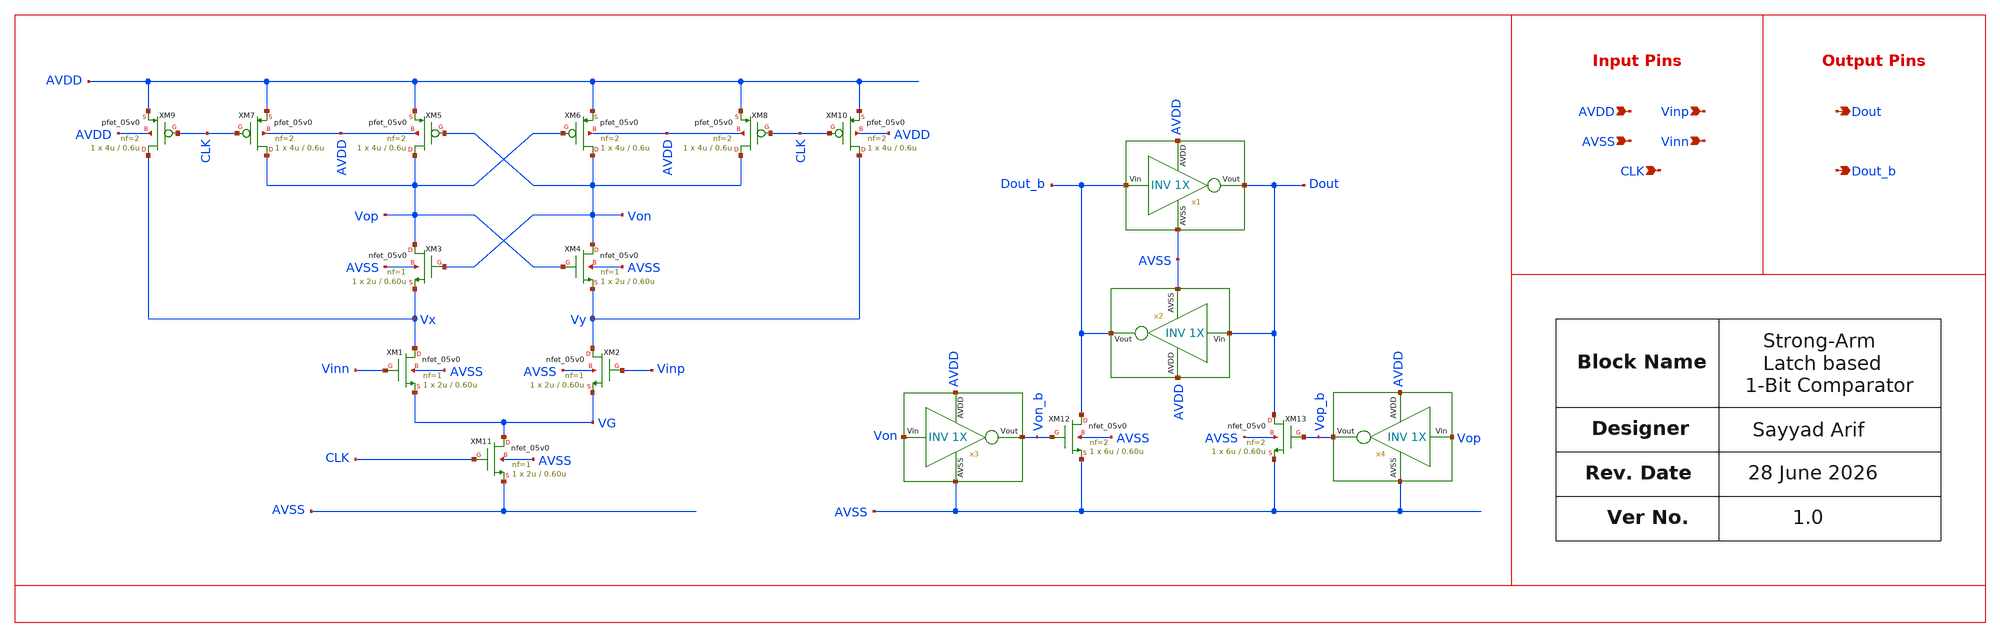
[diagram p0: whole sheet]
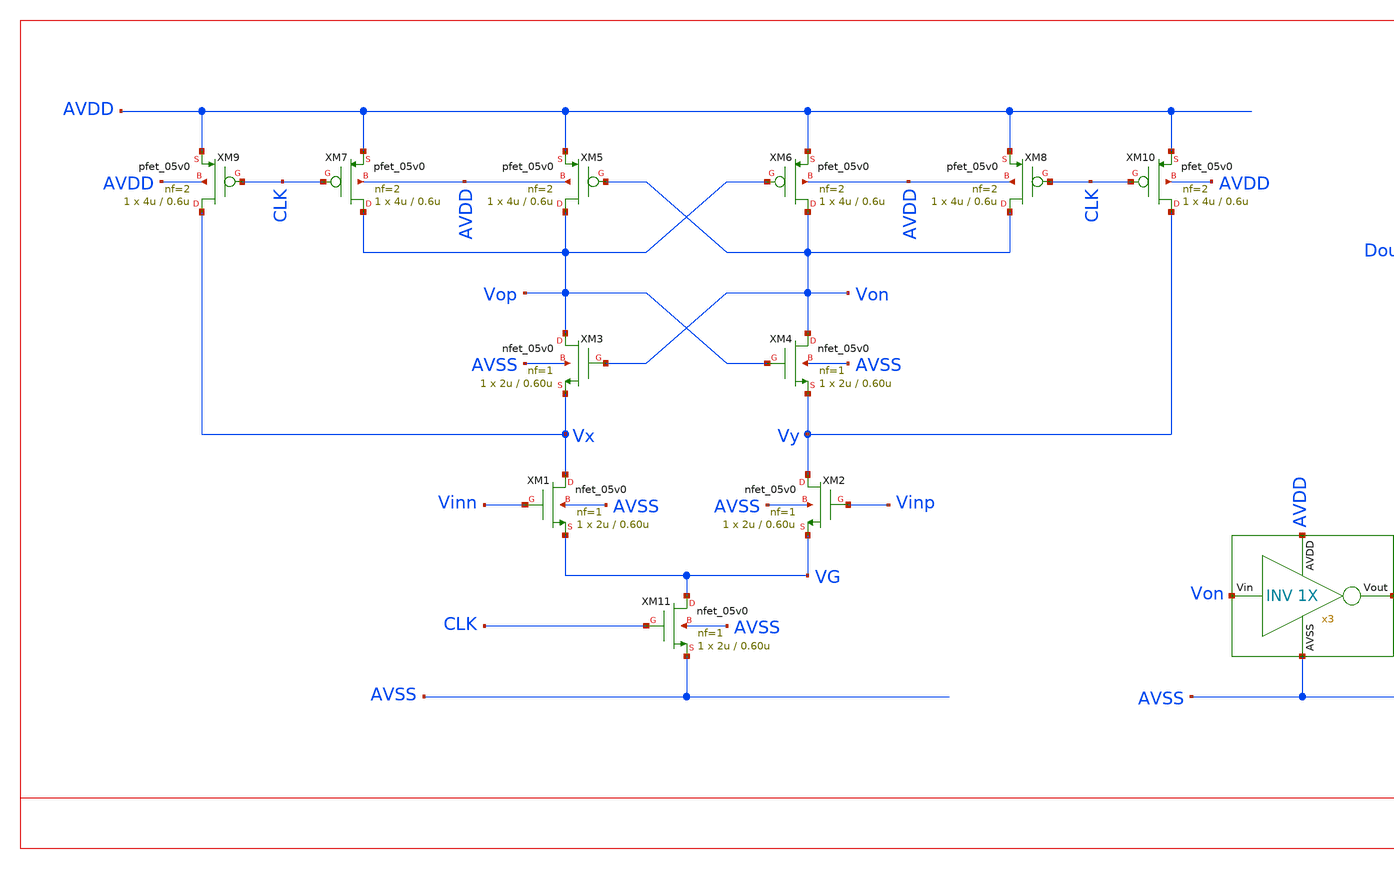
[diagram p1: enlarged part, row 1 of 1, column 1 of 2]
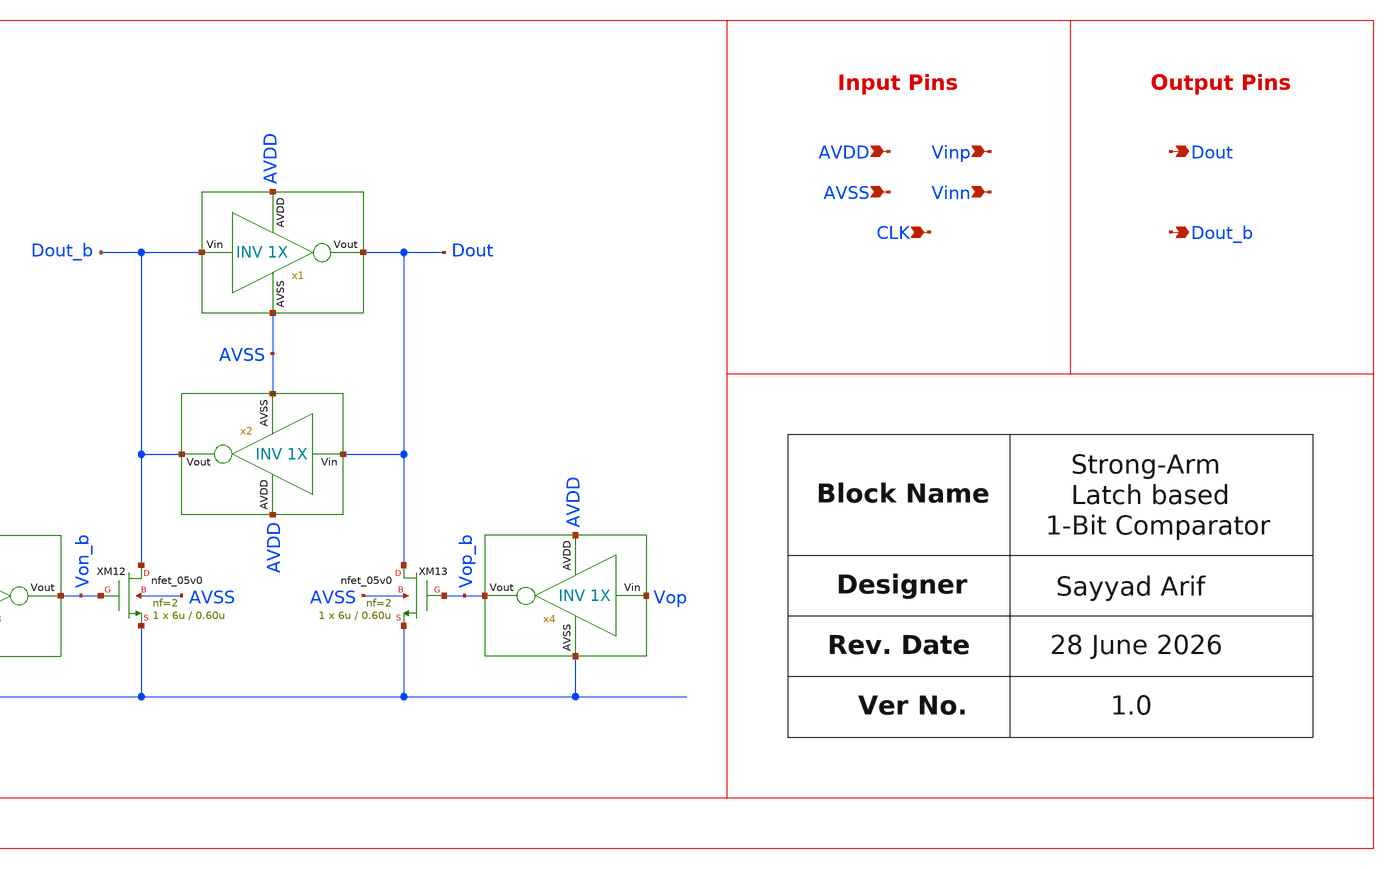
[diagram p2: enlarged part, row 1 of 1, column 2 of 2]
** sch_path: design/schematics/EIS/sa_cic_bms_afe_iadc_quantizer.sch
**.subckt sa_cic_bms_afe_iadc_quantizer Vinn Vinp AVSS AVDD CLK Dout_b Dout
*.ipin Vinn
*.ipin Vinp
*.ipin AVSS
*.ipin AVDD
*.ipin CLK
*.opin Dout_b
*.opin Dout
XM1 Vx Vinn VG AVSS nfet_05v0 L=0.60u W=2u nf=1 ad='int((nf+1)/2) * W/nf * 0.18u' as='int((nf+2)/2) * W/nf * 0.18u'
+ pd='2*int((nf+1)/2) * (W/nf + 0.18u)' ps='2*int((nf+2)/2) * (W/nf + 0.18u)' nrd='0.18u / W' nrs='0.18u / W'
+ sa=0 sb=0 sd=0 m=1
XM2 Vy Vinp VG AVSS nfet_05v0 L=0.60u W=2u nf=1 ad='int((nf+1)/2) * W/nf * 0.18u' as='int((nf+2)/2) * W/nf * 0.18u'
+ pd='2*int((nf+1)/2) * (W/nf + 0.18u)' ps='2*int((nf+2)/2) * (W/nf + 0.18u)' nrd='0.18u / W' nrs='0.18u / W'
+ sa=0 sb=0 sd=0 m=1
XM3 Vop Von Vx AVSS nfet_05v0 L=0.60u W=2u nf=1 ad='int((nf+1)/2) * W/nf * 0.18u' as='int((nf+2)/2) * W/nf * 0.18u'
+ pd='2*int((nf+1)/2) * (W/nf + 0.18u)' ps='2*int((nf+2)/2) * (W/nf + 0.18u)' nrd='0.18u / W' nrs='0.18u / W'
+ sa=0 sb=0 sd=0 m=1
XM4 Von Vop Vy AVSS nfet_05v0 L=0.60u W=2u nf=1 ad='int((nf+1)/2) * W/nf * 0.18u' as='int((nf+2)/2) * W/nf * 0.18u'
+ pd='2*int((nf+1)/2) * (W/nf + 0.18u)' ps='2*int((nf+2)/2) * (W/nf + 0.18u)' nrd='0.18u / W' nrs='0.18u / W'
+ sa=0 sb=0 sd=0 m=1
XM5 Vop Von AVDD AVDD pfet_05v0 L=0.6u W=4u nf=2 ad='int((nf+1)/2) * W/nf * 0.18u' as='int((nf+2)/2) * W/nf * 0.18u'
+ pd='2*int((nf+1)/2) * (W/nf + 0.18u)' ps='2*int((nf+2)/2) * (W/nf + 0.18u)' nrd='0.18u / W' nrs='0.18u / W'
+ sa=0 sb=0 sd=0 m=1
XM6 Von Vop AVDD AVDD pfet_05v0 L=0.6u W=4u nf=2 ad='int((nf+1)/2) * W/nf * 0.18u' as='int((nf+2)/2) * W/nf * 0.18u'
+ pd='2*int((nf+1)/2) * (W/nf + 0.18u)' ps='2*int((nf+2)/2) * (W/nf + 0.18u)' nrd='0.18u / W' nrs='0.18u / W'
+ sa=0 sb=0 sd=0 m=1
XM7 Vop CLK AVDD AVDD pfet_05v0 L=0.6u W=4u nf=2 ad='int((nf+1)/2) * W/nf * 0.18u' as='int((nf+2)/2) * W/nf * 0.18u'
+ pd='2*int((nf+1)/2) * (W/nf + 0.18u)' ps='2*int((nf+2)/2) * (W/nf + 0.18u)' nrd='0.18u / W' nrs='0.18u / W'
+ sa=0 sb=0 sd=0 m=1
XM8 Von CLK AVDD AVDD pfet_05v0 L=0.6u W=4u nf=2 ad='int((nf+1)/2) * W/nf * 0.18u' as='int((nf+2)/2) * W/nf * 0.18u'
+ pd='2*int((nf+1)/2) * (W/nf + 0.18u)' ps='2*int((nf+2)/2) * (W/nf + 0.18u)' nrd='0.18u / W' nrs='0.18u / W'
+ sa=0 sb=0 sd=0 m=1
XM9 Vx CLK AVDD AVDD pfet_05v0 L=0.6u W=4u nf=2 ad='int((nf+1)/2) * W/nf * 0.18u' as='int((nf+2)/2) * W/nf * 0.18u'
+ pd='2*int((nf+1)/2) * (W/nf + 0.18u)' ps='2*int((nf+2)/2) * (W/nf + 0.18u)' nrd='0.18u / W' nrs='0.18u / W'
+ sa=0 sb=0 sd=0 m=1
XM10 Vy CLK AVDD AVDD pfet_05v0 L=0.6u W=4u nf=2 ad='int((nf+1)/2) * W/nf * 0.18u' as='int((nf+2)/2) * W/nf * 0.18u'
+ pd='2*int((nf+1)/2) * (W/nf + 0.18u)' ps='2*int((nf+2)/2) * (W/nf + 0.18u)' nrd='0.18u / W' nrs='0.18u / W'
+ sa=0 sb=0 sd=0 m=1
XM11 VG CLK AVSS AVSS nfet_05v0 L=0.60u W=2u nf=1 ad='int((nf+1)/2) * W/nf * 0.18u' as='int((nf+2)/2) * W/nf * 0.18u'
+ pd='2*int((nf+1)/2) * (W/nf + 0.18u)' ps='2*int((nf+2)/2) * (W/nf + 0.18u)' nrd='0.18u / W' nrs='0.18u / W'
+ sa=0 sb=0 sd=0 m=1
XM12 Dout_b Von_b AVSS AVSS nfet_05v0 L=0.60u W=6u nf=2 ad='int((nf+1)/2) * W/nf * 0.18u' as='int((nf+2)/2) * W/nf * 0.18u'
+ pd='2*int((nf+1)/2) * (W/nf + 0.18u)' ps='2*int((nf+2)/2) * (W/nf + 0.18u)' nrd='0.18u / W' nrs='0.18u / W'
+ sa=0 sb=0 sd=0 m=1
XM13 Dout Vop_b AVSS AVSS nfet_05v0 L=0.60u W=6u nf=2 ad='int((nf+1)/2) * W/nf * 0.18u' as='int((nf+2)/2) * W/nf * 0.18u'
+ pd='2*int((nf+1)/2) * (W/nf + 0.18u)' ps='2*int((nf+2)/2) * (W/nf + 0.18u)' nrd='0.18u / W' nrs='0.18u / W'
+ sa=0 sb=0 sd=0 m=1
x1 AVDD Dout Dout_b AVSS sa_cic_bms_afe_iadc_quantizer_inv1x
x2 AVDD Dout_b Dout AVSS sa_cic_bms_afe_iadc_quantizer_inv1x
x3 AVDD Von_b Von AVSS sa_cic_bms_afe_iadc_quantizer_inv1x
x4 AVDD Vop_b Vop AVSS sa_cic_bms_afe_iadc_quantizer_inv1x
**.ends
.end
